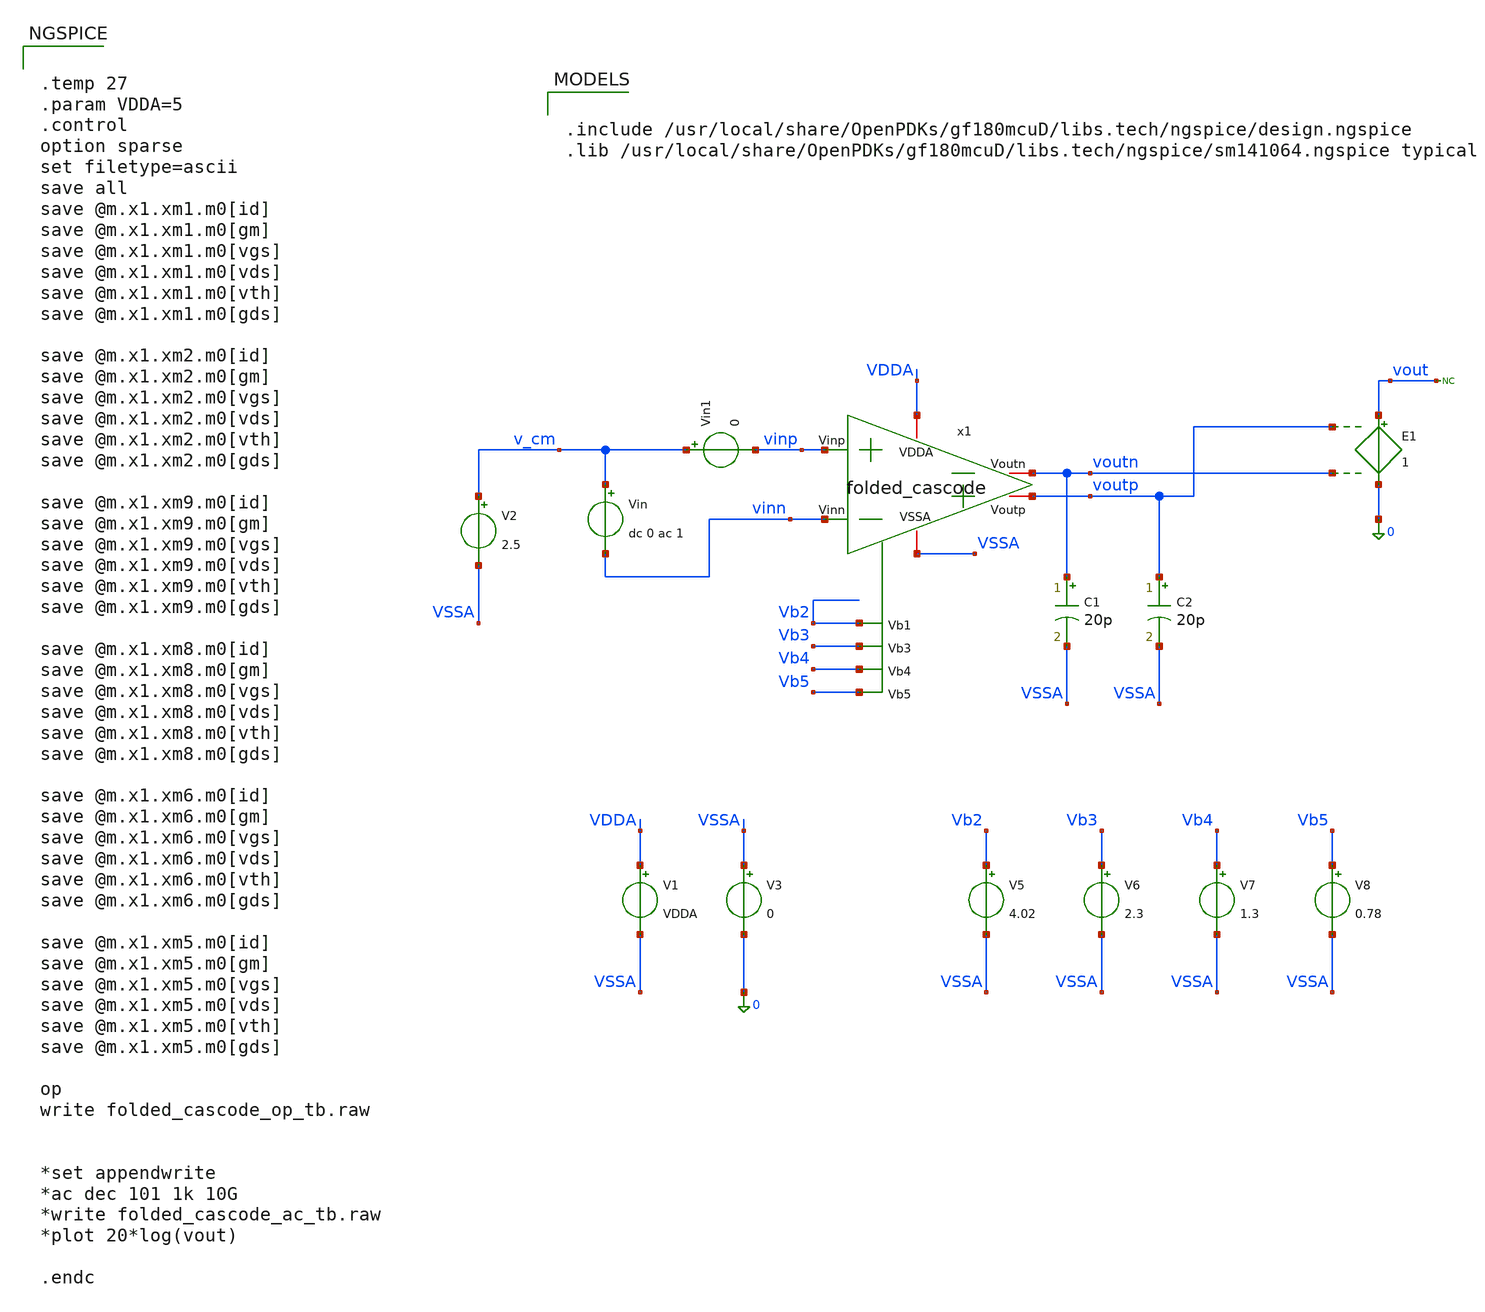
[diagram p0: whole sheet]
** sch_path: Folded_cascode/testbenches/simulation/folded_cascode_op_tb_batch.sch
**.subckt folded_cascode_op_tb_batch
x1 VDDA VSSA vinp vinn voutp voutn Vb2 Vb3 Vb4 Vb5 folded_cascode
V1 VDDA VSSA VDDA
Vin1 v_cm vinp 0
Vin v_cm vinn dc 0 ac 1
C1 voutn VSSA 20p m=1
C2 voutp VSSA 20p m=1
V2 v_cm VSSA 2.5
V3 VSSA 0 0
E1 vout 0 voutp voutn 1
V5 Vb2 VSSA 4.02
V6 Vb3 VSSA 2.3
V7 Vb4 VSSA 1.3
V8 Vb5 VSSA 0.78
* noconn vout
**** begin user architecture code


.temp 27
.param VDDA=5
.control
option sparse
set filetype=ascii
save all
save @m.x1.xm1.m0[id]
save @m.x1.xm1.m0[gm]
save @m.x1.xm1.m0[vgs]
save @m.x1.xm1.m0[vds]
save @m.x1.xm1.m0[vth]
save @m.x1.xm1.m0[gds]

save @m.x1.xm2.m0[id]
save @m.x1.xm2.m0[gm]
save @m.x1.xm2.m0[vgs]
save @m.x1.xm2.m0[vds]
save @m.x1.xm2.m0[vth]
save @m.x1.xm2.m0[gds]

save @m.x1.xm9.m0[id]
save @m.x1.xm9.m0[gm]
save @m.x1.xm9.m0[vgs]
save @m.x1.xm9.m0[vds]
save @m.x1.xm9.m0[vth]
save @m.x1.xm9.m0[gds]

save @m.x1.xm8.m0[id]
save @m.x1.xm8.m0[gm]
save @m.x1.xm8.m0[vgs]
save @m.x1.xm8.m0[vds]
save @m.x1.xm8.m0[vth]
save @m.x1.xm8.m0[gds]

save @m.x1.xm6.m0[id]
save @m.x1.xm6.m0[gm]
save @m.x1.xm6.m0[vgs]
save @m.x1.xm6.m0[vds]
save @m.x1.xm6.m0[vth]
save @m.x1.xm6.m0[gds]

save @m.x1.xm5.m0[id]
save @m.x1.xm5.m0[gm]
save @m.x1.xm5.m0[vgs]
save @m.x1.xm5.m0[vds]
save @m.x1.xm5.m0[vth]
save @m.x1.xm5.m0[gds]

op
write folded_cascode_op_tb.raw


*set appendwrite
*ac dec 101 1k 10G
*write folded_cascode_ac_tb.raw
*plot 20*log(vout)

.endc



.include /usr/local/share/OpenPDKs/gf180mcuD/libs.tech/ngspice/design.ngspice
.lib /usr/local/share/OpenPDKs/gf180mcuD/libs.tech/ngspice/sm141064.ngspice typical

**** end user architecture code
**.ends
.end
